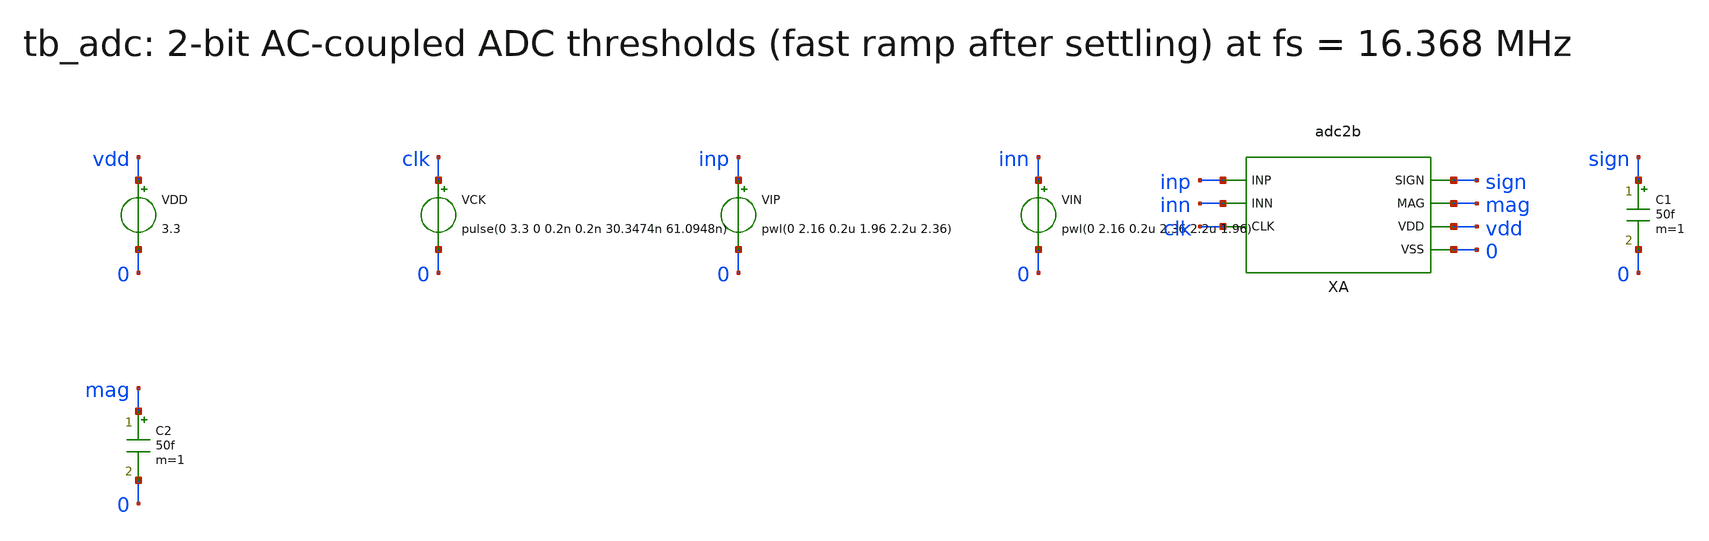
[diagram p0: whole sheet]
** sch_path: xschem/tb_adc.sch
**.subckt tb_adc
VDD vdd 0 3.3
VCK clk 0 pulse(0 3.3 0 0.2n 0.2n 30.3474n 61.0948n)
VIP inp 0 pwl(0 2.16 0.2u 1.96 2.2u 2.36)
VIN inn 0 pwl(0 2.16 0.2u 2.36 2.2u 1.96)
XA inp inn clk sign mag vdd 0 adc2b
C1 sign 0 50f m=1
C2 mag 0 50f m=1
**** begin user architecture code
 .include $::180MCU_MODELS/design.ngspice
.lib $::180MCU_MODELS/sm141064.ngspice typical
.lib $::180MCU_MODELS/sm141064.ngspice res_typical
.lib $::180MCU_MODELS/sm141064.ngspice mimcap_typical

.control
set num_threads=1
tran 0.1n 2.2u
let vd = v(xa.inp_i)-v(xa.inn_i)
meas tran ts when v(sign)=1.65 rise=1 td=0.3u
meas tran tm1 when v(mag)=1.65 fall=1 td=0.3u
meas tran tm2 when v(mag)=1.65 rise=1 td=0.3u
meas tran vs find vd at=ts
meas tran vm1 find vd at=tm1
meas tran vm2 find vd at=tm2
echo RES vth_sign=$&vs vth_mag_lo=$&vm1 vth_mag_hi=$&vm2
meas tran thp avg v(xa.thp) from=0.5u to=2u
meas tran thm avg v(xa.thm) from=0.5u to=2u
meas tran thn avg v(xa.thn) from=0.5u to=2u
echo RES ladder thp=$&thp thm=$&thm thn=$&thn
meas tran iavg avg i(VDD) from=0.5u to=2u
echo RES iavg=$&iavg
.endc

**** end user architecture code
**.ends
.end
